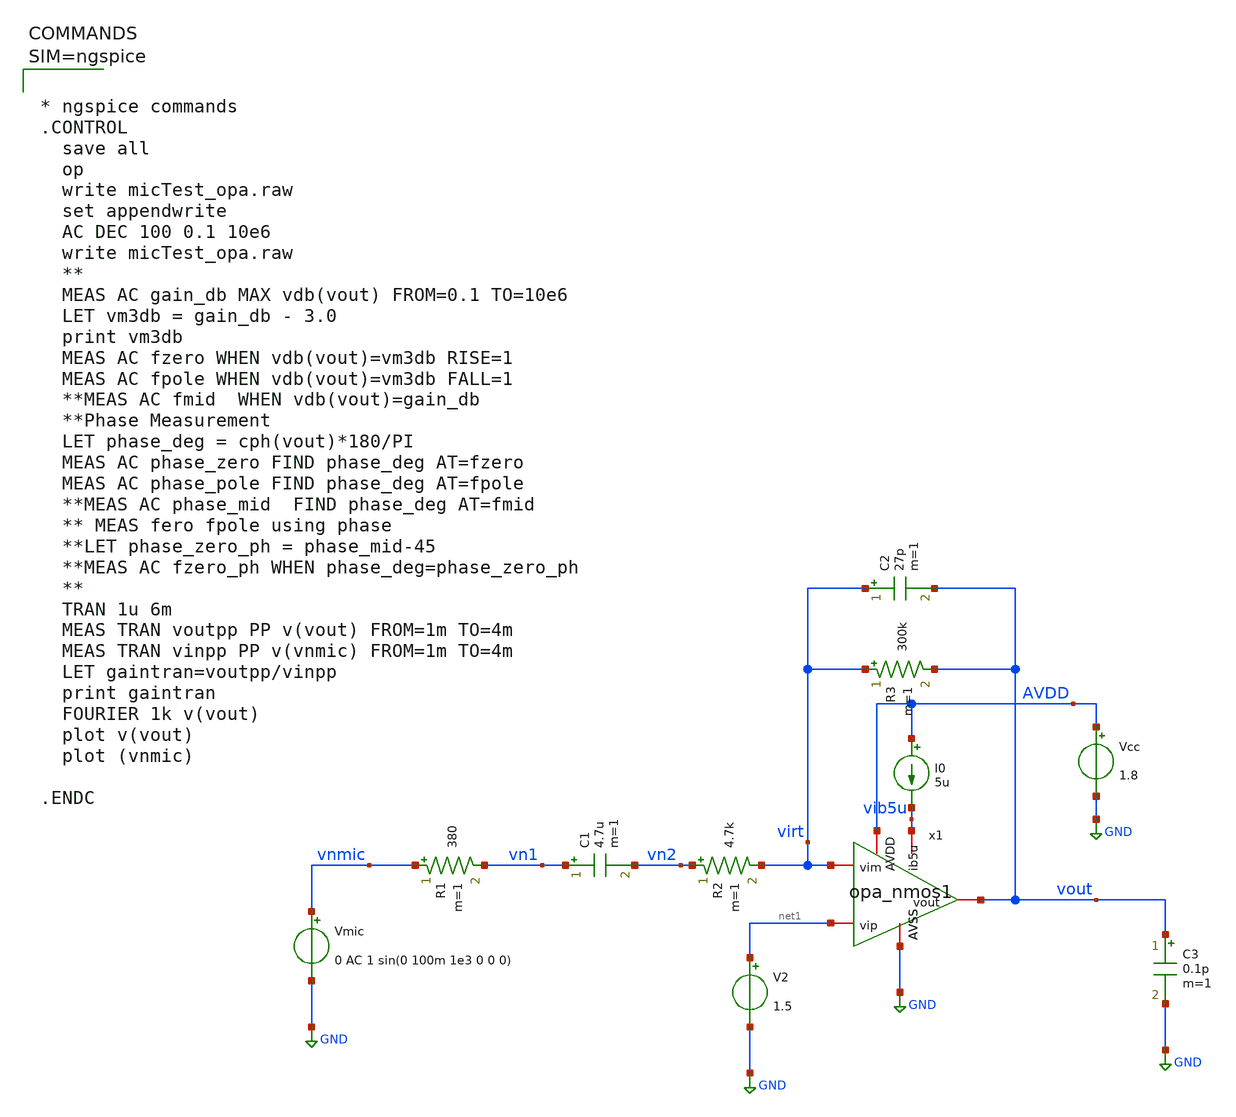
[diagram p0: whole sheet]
** sch_path: xschem/micTest_opa_nmos.sch
**.subckt micTest_opa_nmos
Vmic vnmic GND 0 AC 1 sin(0 100m 1e3 0 0 0)
R1 vnmic vn1 380 m=1
C1 vn1 vn2 4.7u m=1
R2 vn2 virt 4.7k m=1
R3 virt vout 300k m=1
C2 virt vout 27p m=1
V2 net1 GND 1.5
C3 vout GND 0.1p m=1
x1 vout net1 virt GND AVDD vib5u opa_nmos1
Vcc AVDD GND 1.8
I0 AVDD vib5u 5u
**** begin user architecture code



* ngspice commands
.CONTROL
  save all
  op
  write micTest_opa.raw
  set appendwrite
  AC DEC 100 0.1 10e6
  write micTest_opa.raw
  **
  MEAS AC gain_db MAX vdb(vout) FROM=0.1 TO=10e6
  LET vm3db = gain_db - 3.0
  print vm3db
  MEAS AC fzero WHEN vdb(vout)=vm3db RISE=1
  MEAS AC fpole WHEN vdb(vout)=vm3db FALL=1
  **MEAS AC fmid  WHEN vdb(vout)=gain_db
  **Phase Measurement
  LET phase_deg = cph(vout)*180/PI
  MEAS AC phase_zero FIND phase_deg AT=fzero
  MEAS AC phase_pole FIND phase_deg AT=fpole
  **MEAS AC phase_mid  FIND phase_deg AT=fmid
  ** MEAS fero fpole using phase
  **LET phase_zero_ph = phase_mid-45
  **MEAS AC fzero_ph WHEN phase_deg=phase_zero_ph
  **
  TRAN 1u 6m
  MEAS TRAN voutpp PP v(vout) FROM=1m TO=4m
  MEAS TRAN vinpp PP v(vnmic) FROM=1m TO=4m
  LET gaintran=voutpp/vinpp
  print gaintran
  FOURIER 1k v(vout)
  plot v(vout)
  plot (vnmic)

.ENDC




** opencircuitdesign pdks install
.lib $::SKYWATER_MODELS/sky130.lib.spice tt

**** end user architecture code
**.ends

* expanding   symbol:  opa_nmos1.sym # of pins=6
** sym_path: xschem/opa_nmos1.sym
** sch_path: xschem/opa_nmos1.sch
.subckt opa_nmos1 vout vip vim AVSS AVDD ib5u
*.iopin vip
*.iopin vim
*.iopin AVDD
*.iopin AVSS
*.iopin ib5u
*.iopin vout
XMtail vs ib5u AVSS AVSS sky130_fd_pr__nfet_01v8 L=1 W=5 nf=1 ad='int((1 + 1)/2) * 5 / 1 * 0.29' as='int((1 + 2)/2) * 5 / 1 * 0.29'
+ pd='2*int((1 + 1)/2) * (5 / 1 + 0.29)' ps='2*int((1 + 2)/2) * (5 / 1 + 0.29)' nrd='0.29 / 5 ' nrs='0.29 / 5 '
+ sa=0 sb=0 sd=0 mult=2 m=2
XM1 ib5u ib5u AVSS AVSS sky130_fd_pr__nfet_01v8 L=1 W=5 nf=1 ad='int((1 + 1)/2) * 5 / 1 * 0.29' as='int((1 + 2)/2) * 5 / 1 * 0.29'
+ pd='2*int((1 + 1)/2) * (5 / 1 + 0.29)' ps='2*int((1 + 2)/2) * (5 / 1 + 0.29)' nrd='0.29 / 5 ' nrs='0.29 / 5 '
+ sa=0 sb=0 sd=0 mult=1 m=1
XMip vom vip vs vs sky130_fd_pr__nfet_01v8_lvt L=2 W=5 nf=1 ad='int((1 + 1)/2) * 5 / 1 * 0.29' as='int((1 + 2)/2) * 5 / 1 * 0.29'
+ pd='2*int((1 + 1)/2) * (5 / 1 + 0.29)' ps='2*int((1 + 2)/2) * (5 / 1 + 0.29)' nrd='0.29 / 5 ' nrs='0.29 / 5 '
+ sa=0 sb=0 sd=0 mult=4 m=4
XMim vout vim vs vs sky130_fd_pr__nfet_01v8_lvt L=2 W=5 nf=1 ad='int((1 + 1)/2) * 5 / 1 * 0.29' as='int((1 + 2)/2) * 5 / 1 * 0.29'
+ pd='2*int((1 + 1)/2) * (5 / 1 + 0.29)' ps='2*int((1 + 2)/2) * (5 / 1 + 0.29)' nrd='0.29 / 5 ' nrs='0.29 / 5 '
+ sa=0 sb=0 sd=0 mult=4 m=4
XMpcmm vout vom AVDD AVDD sky130_fd_pr__pfet_01v8_lvt L=2 W=5 nf=1 ad='int((1 + 1)/2) * 5 / 1 * 0.29'
+ as='int((1 + 2)/2) * 5 / 1 * 0.29' pd='2*int((1 + 1)/2) * (5 / 1 + 0.29)' ps='2*int((1 + 2)/2) * (5 / 1 + 0.29)'
+ nrd='0.29 / 5 ' nrs='0.29 / 5 ' sa=0 sb=0 sd=0 mult=2 m=2
XMpcmp vom vom AVDD AVDD sky130_fd_pr__pfet_01v8_lvt L=2 W=5 nf=1 ad='int((1 + 1)/2) * 5 / 1 * 0.29'
+ as='int((1 + 2)/2) * 5 / 1 * 0.29' pd='2*int((1 + 1)/2) * (5 / 1 + 0.29)' ps='2*int((1 + 2)/2) * (5 / 1 + 0.29)'
+ nrd='0.29 / 5 ' nrs='0.29 / 5 ' sa=0 sb=0 sd=0 mult=2 m=2
.ends

.GLOBAL GND
.end
